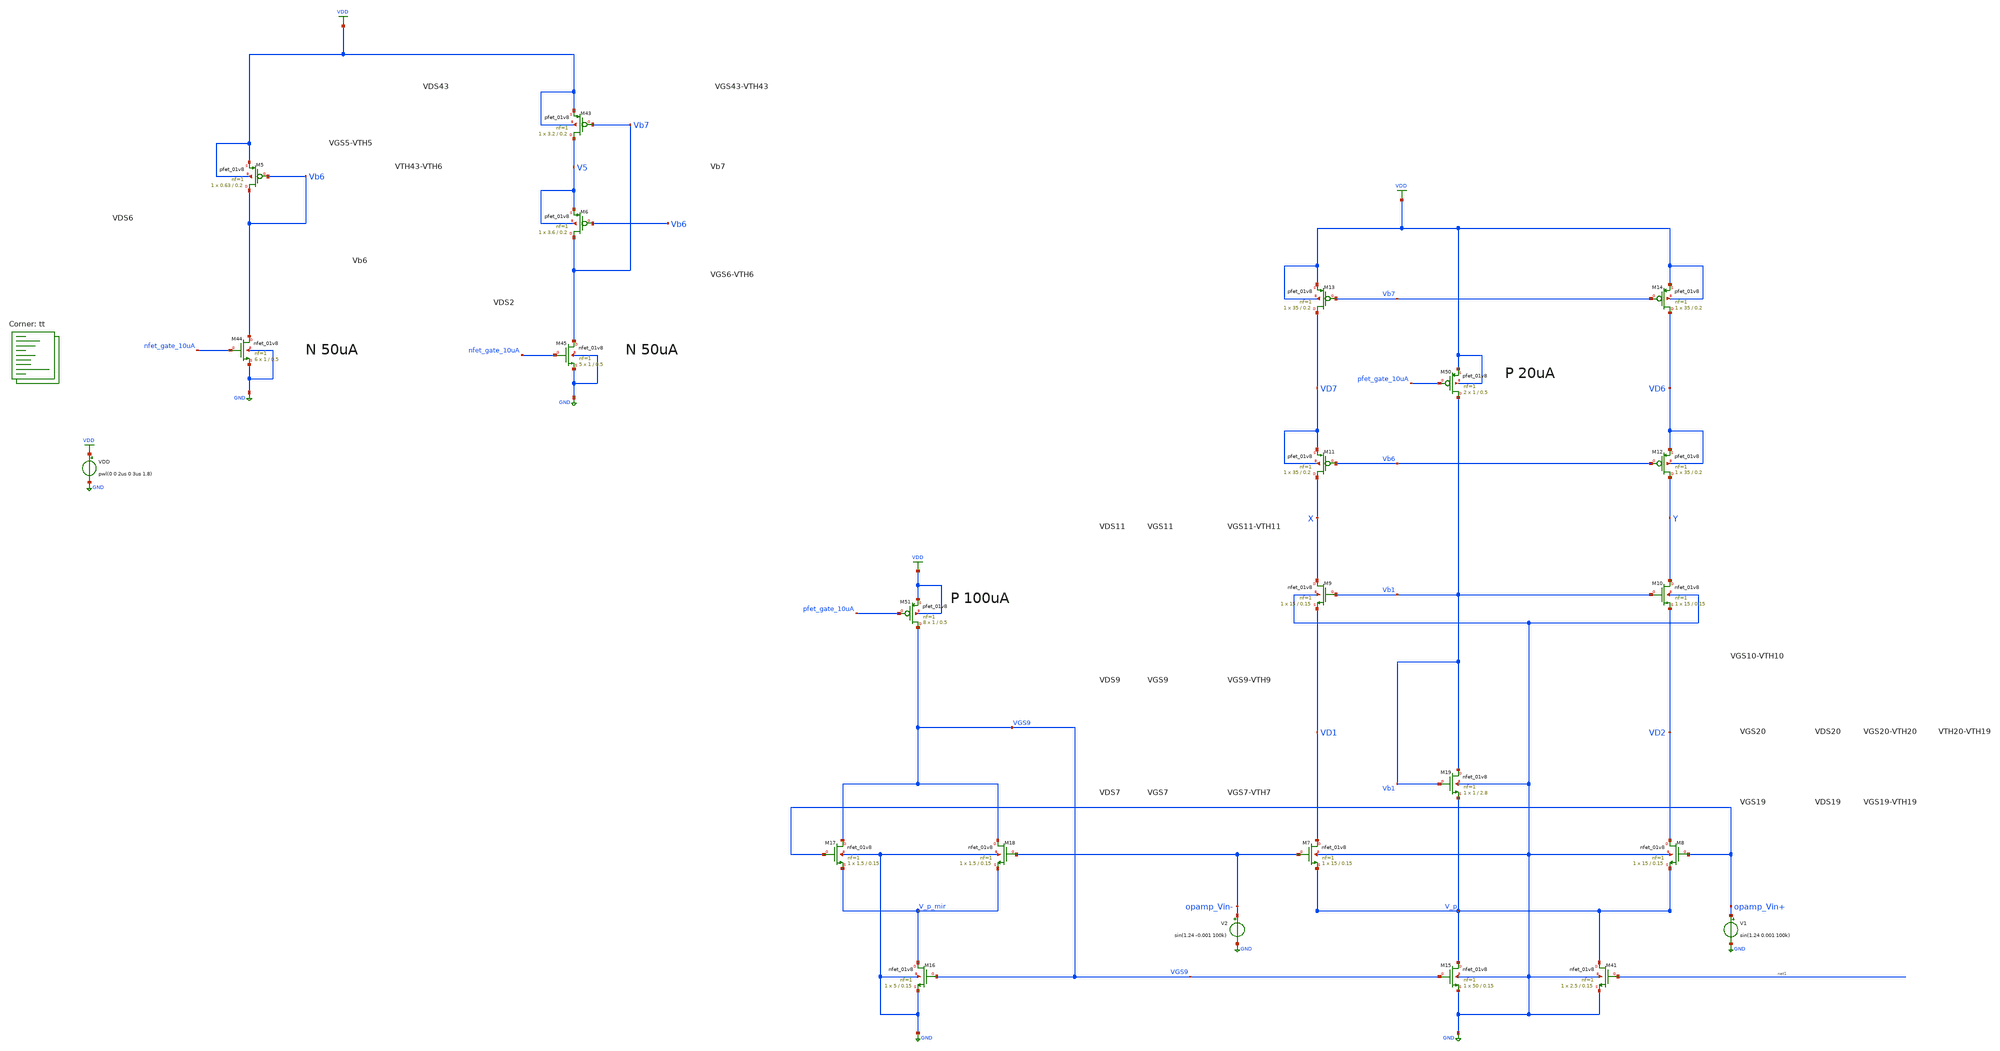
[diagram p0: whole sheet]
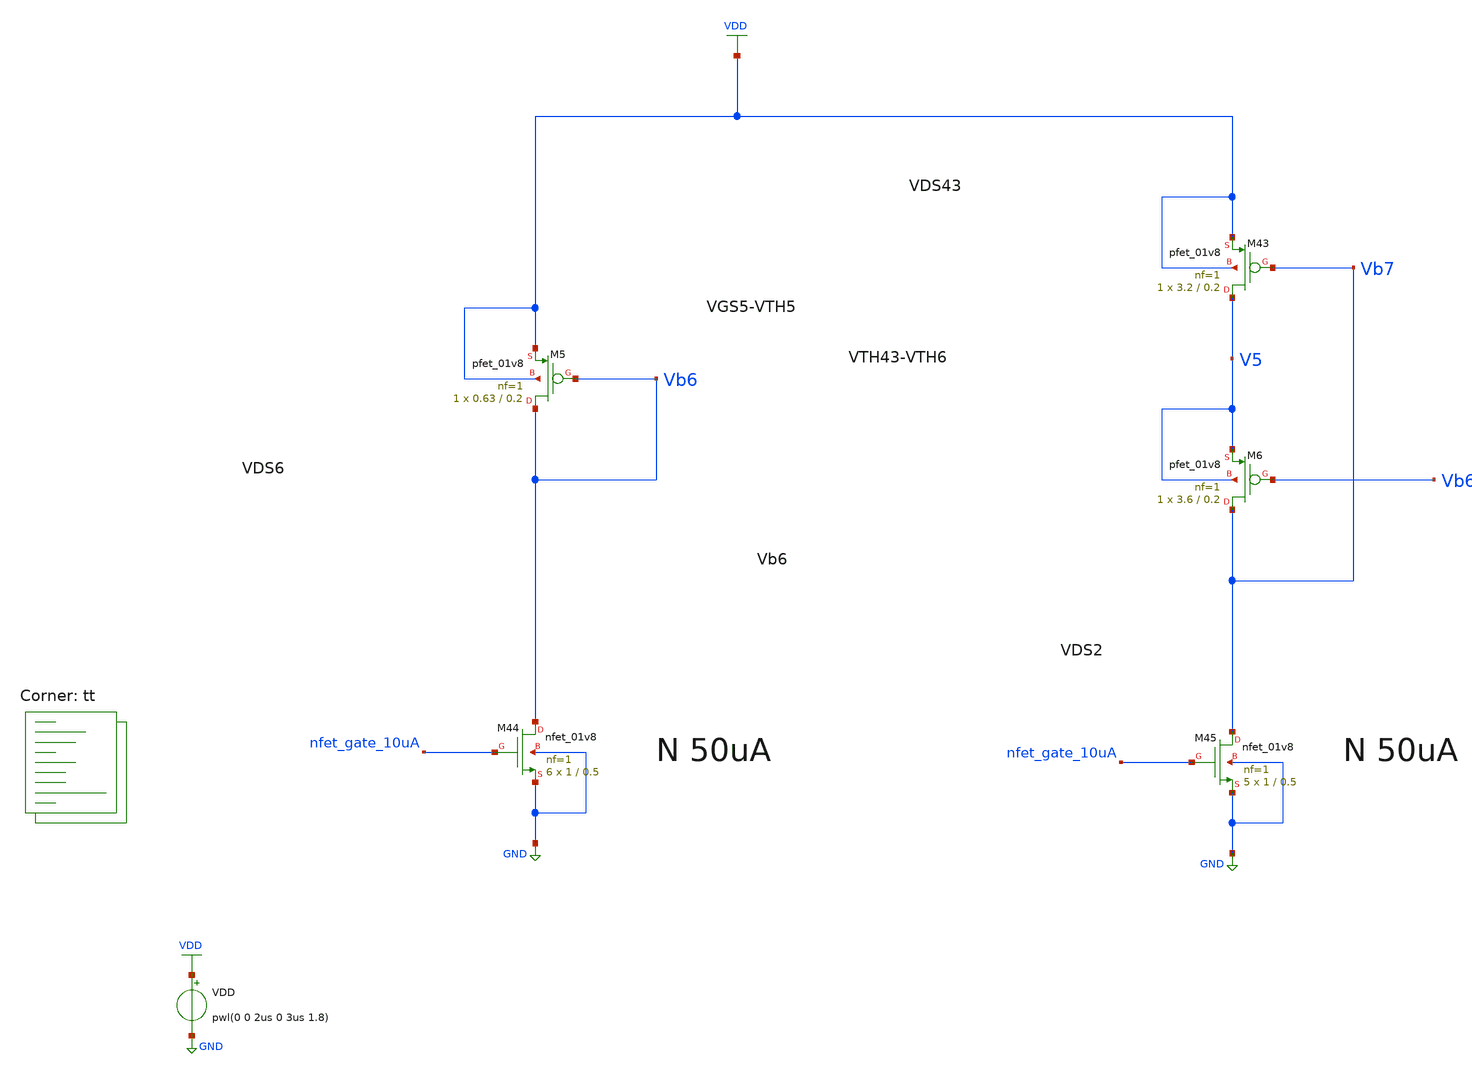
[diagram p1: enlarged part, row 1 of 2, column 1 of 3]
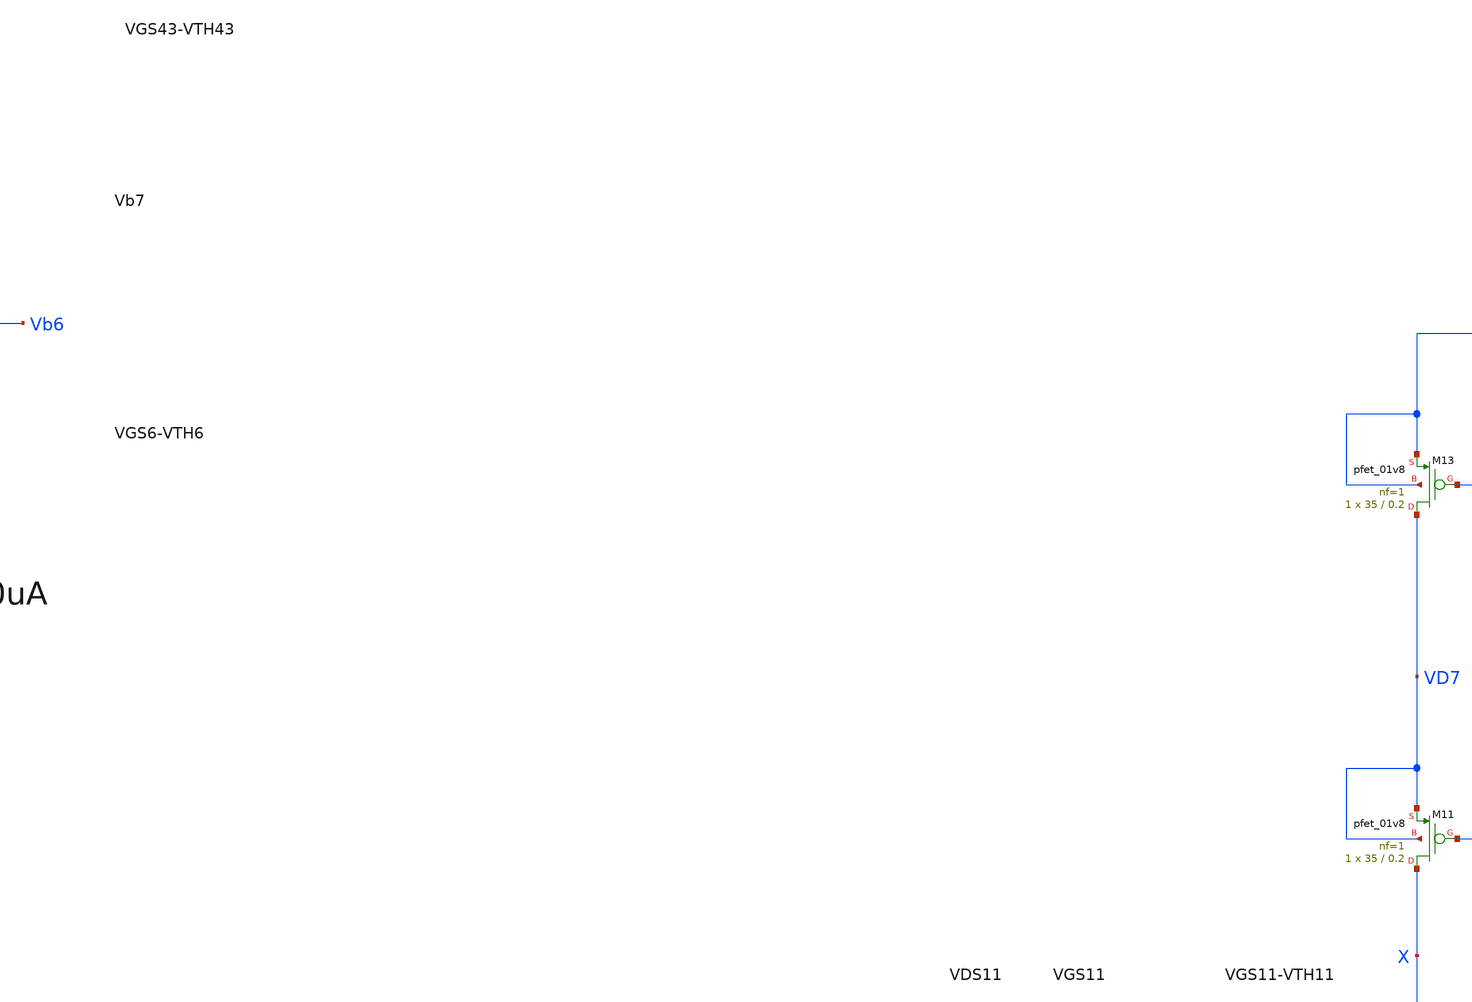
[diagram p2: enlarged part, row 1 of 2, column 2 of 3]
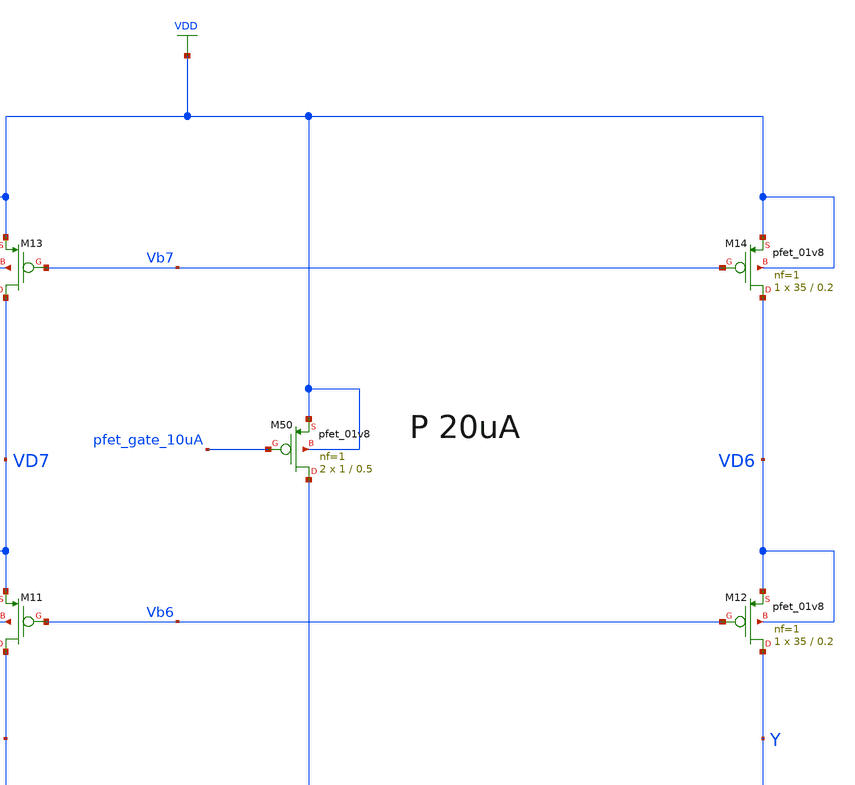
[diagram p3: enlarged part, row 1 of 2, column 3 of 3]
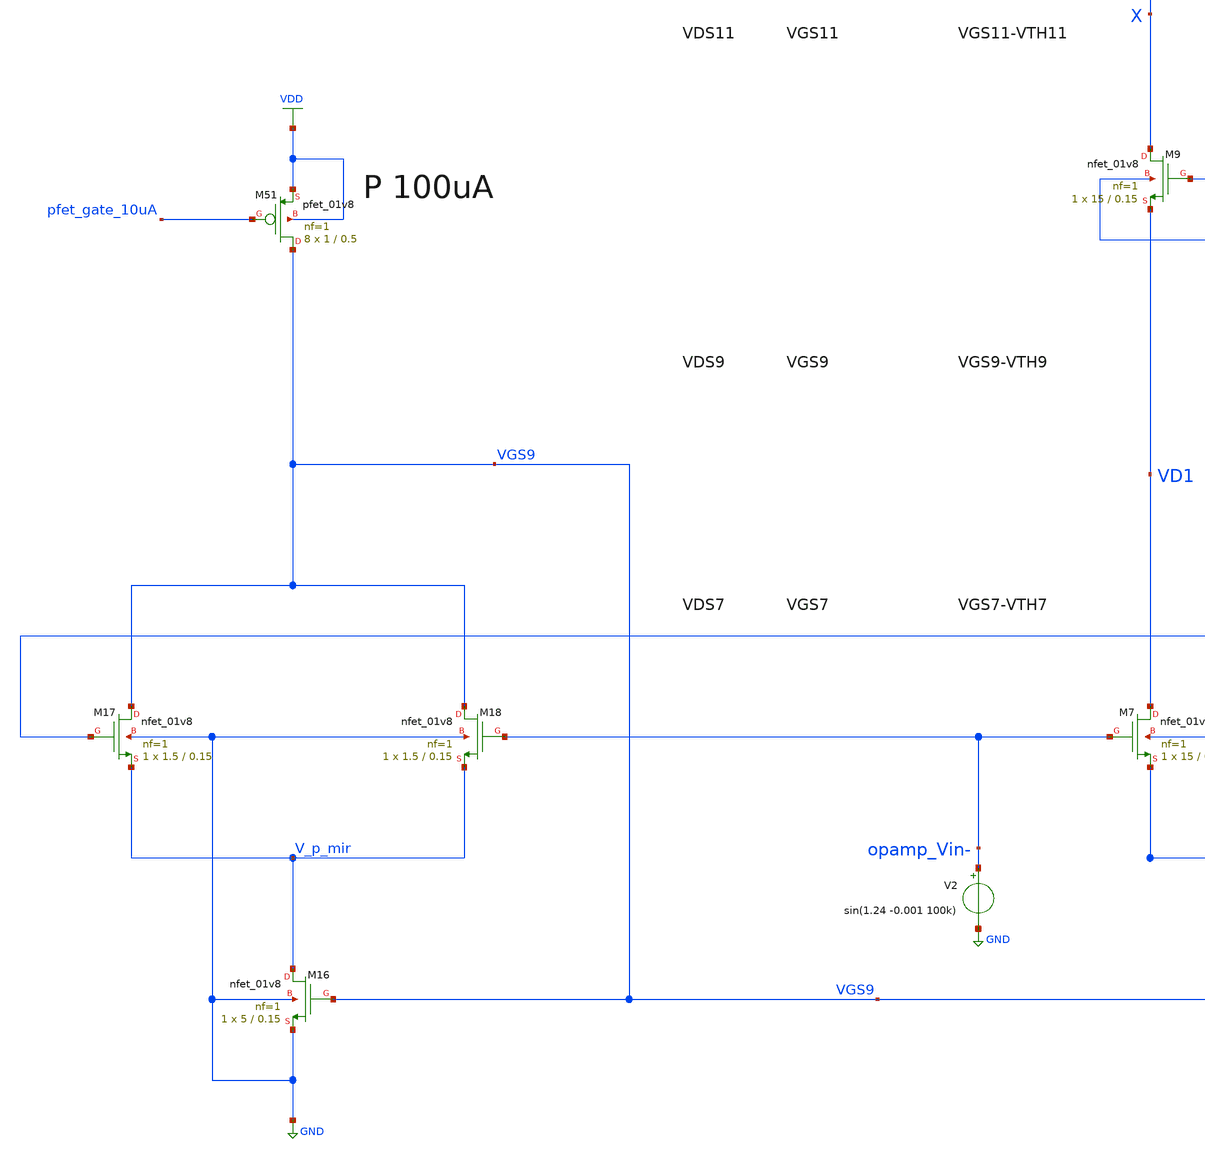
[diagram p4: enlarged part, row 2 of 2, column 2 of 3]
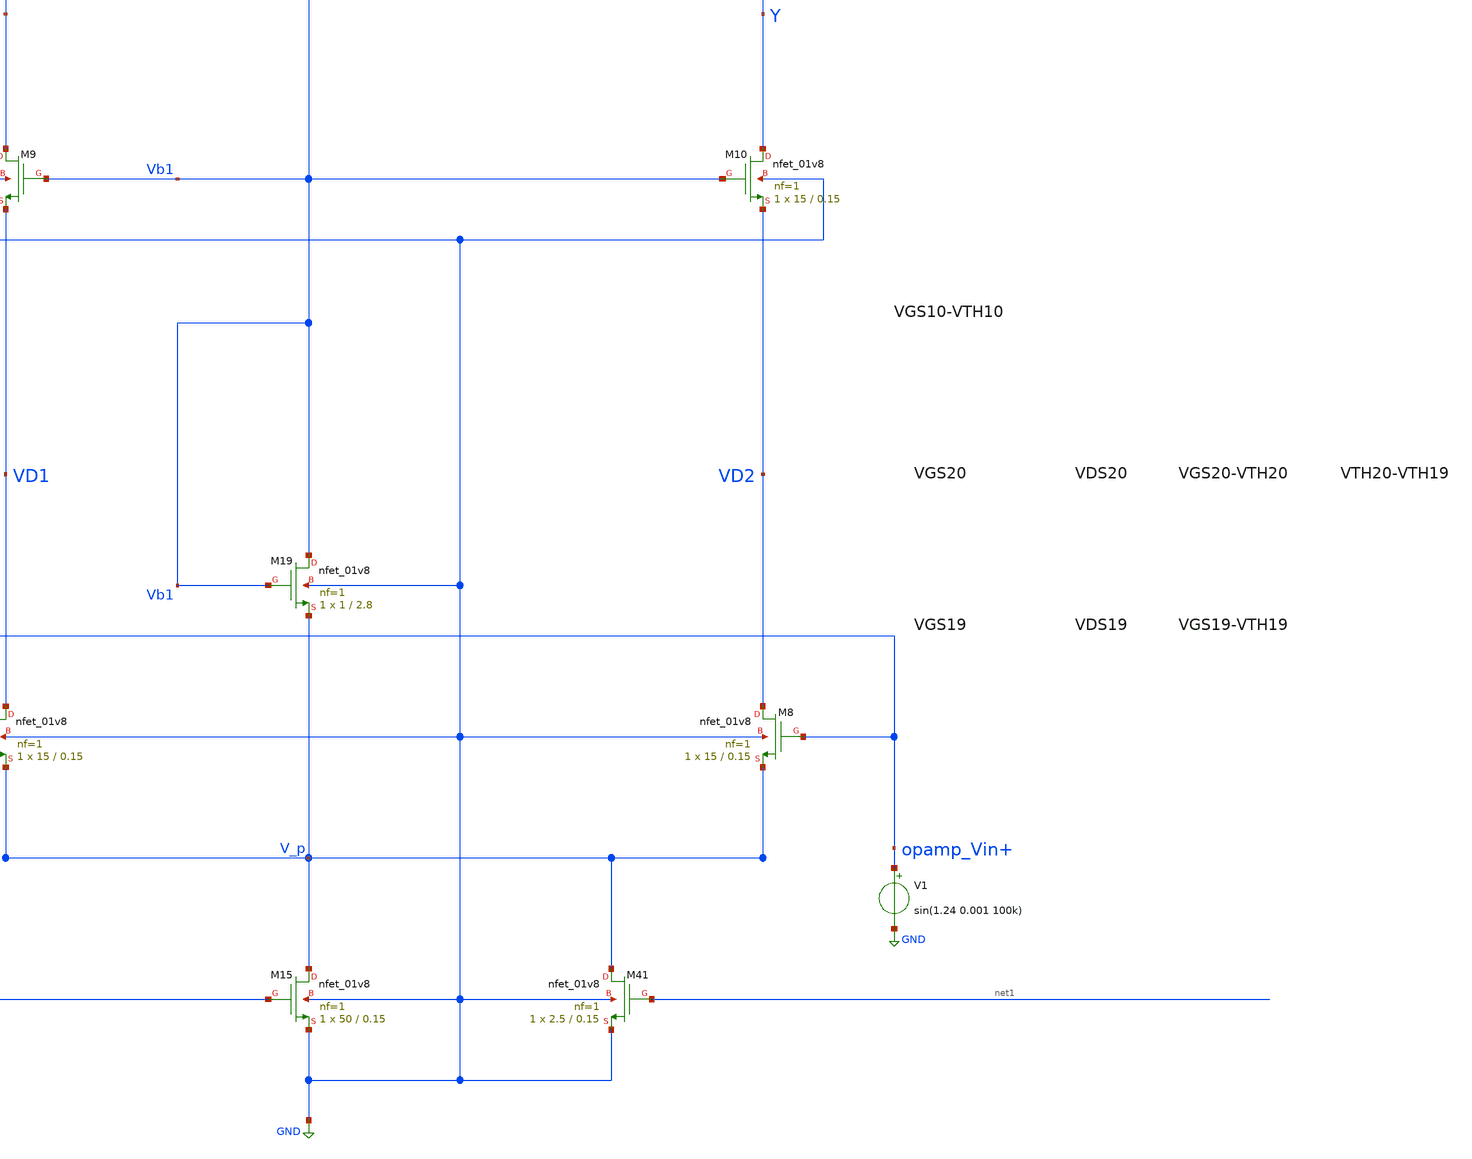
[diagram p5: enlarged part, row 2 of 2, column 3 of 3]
** sch_path: projects/ASU/EEE572/schematic/tb_opamp_full_5_2.sch
**.subckt tb_opamp_full_5_2
VDD VDD GND pwl(0 0 2us 0 3us 1.8)
XM7 VD1 opamp_Vin- V_p GND sky130_fd_pr__nfet_01v8 L=0.15 W=15 nf=1 ad='int((nf+1)/2) * W/nf * 0.29'
+ as='int((nf+2)/2) * W/nf * 0.29' pd='2*int((nf+1)/2) * (W/nf + 0.29)' ps='2*int((nf+2)/2) * (W/nf + 0.29)'
+ nrd='0.29 / W' nrs='0.29 / W' sa=0 sb=0 sd=0 mult=1 m=1
XM8 VD2 opamp_Vin+ V_p GND sky130_fd_pr__nfet_01v8 L=0.15 W=15 nf=1 ad='int((nf+1)/2) * W/nf * 0.29'
+ as='int((nf+2)/2) * W/nf * 0.29' pd='2*int((nf+1)/2) * (W/nf + 0.29)' ps='2*int((nf+2)/2) * (W/nf + 0.29)'
+ nrd='0.29 / W' nrs='0.29 / W' sa=0 sb=0 sd=0 mult=1 m=1
XM9 X Vb1 VD1 GND sky130_fd_pr__nfet_01v8 L=0.15 W=15 nf=1 ad='int((nf+1)/2) * W/nf * 0.29' as='int((nf+2)/2) * W/nf * 0.29'
+ pd='2*int((nf+1)/2) * (W/nf + 0.29)' ps='2*int((nf+2)/2) * (W/nf + 0.29)' nrd='0.29 / W' nrs='0.29 / W'
+ sa=0 sb=0 sd=0 mult=1 m=1
XM10 Y Vb1 VD2 GND sky130_fd_pr__nfet_01v8 L=0.15 W=15 nf=1 ad='int((nf+1)/2) * W/nf * 0.29' as='int((nf+2)/2) * W/nf * 0.29'
+ pd='2*int((nf+1)/2) * (W/nf + 0.29)' ps='2*int((nf+2)/2) * (W/nf + 0.29)' nrd='0.29 / W' nrs='0.29 / W'
+ sa=0 sb=0 sd=0 mult=1 m=1
XM11 X Vb6 VD7 VD7 sky130_fd_pr__pfet_01v8 L=0.2 W=35 nf=1 ad='int((nf+1)/2) * W/nf * 0.29' as='int((nf+2)/2) * W/nf * 0.29'
+ pd='2*int((nf+1)/2) * (W/nf + 0.29)' ps='2*int((nf+2)/2) * (W/nf + 0.29)' nrd='0.29 / W' nrs='0.29 / W'
+ sa=0 sb=0 sd=0 mult=1 m=1
XM12 Y Vb6 VD6 VD6 sky130_fd_pr__pfet_01v8 L=0.2 W=35 nf=1 ad='int((nf+1)/2) * W/nf * 0.29' as='int((nf+2)/2) * W/nf * 0.29'
+ pd='2*int((nf+1)/2) * (W/nf + 0.29)' ps='2*int((nf+2)/2) * (W/nf + 0.29)' nrd='0.29 / W' nrs='0.29 / W'
+ sa=0 sb=0 sd=0 mult=1 m=1
XM13 VD7 Vb7 VDD VDD sky130_fd_pr__pfet_01v8 L=0.2 W=35 nf=1 ad='int((nf+1)/2) * W/nf * 0.29' as='int((nf+2)/2) * W/nf * 0.29'
+ pd='2*int((nf+1)/2) * (W/nf + 0.29)' ps='2*int((nf+2)/2) * (W/nf + 0.29)' nrd='0.29 / W' nrs='0.29 / W'
+ sa=0 sb=0 sd=0 mult=1 m=1
XM14 VD6 Vb7 VDD VDD sky130_fd_pr__pfet_01v8 L=0.2 W=35 nf=1 ad='int((nf+1)/2) * W/nf * 0.29' as='int((nf+2)/2) * W/nf * 0.29'
+ pd='2*int((nf+1)/2) * (W/nf + 0.29)' ps='2*int((nf+2)/2) * (W/nf + 0.29)' nrd='0.29 / W' nrs='0.29 / W'
+ sa=0 sb=0 sd=0 mult=1 m=1
XM15 V_p VGS9 GND GND sky130_fd_pr__nfet_01v8 L=0.15 W=50 nf=1 ad='int((nf+1)/2) * W/nf * 0.29' as='int((nf+2)/2) * W/nf * 0.29'
+ pd='2*int((nf+1)/2) * (W/nf + 0.29)' ps='2*int((nf+2)/2) * (W/nf + 0.29)' nrd='0.29 / W' nrs='0.29 / W'
+ sa=0 sb=0 sd=0 mult=1 m=1
XM16 V_p_mir VGS9 GND GND sky130_fd_pr__nfet_01v8 L=0.15 W=5 nf=1 ad='int((nf+1)/2) * W/nf * 0.29' as='int((nf+2)/2) * W/nf * 0.29'
+ pd='2*int((nf+1)/2) * (W/nf + 0.29)' ps='2*int((nf+2)/2) * (W/nf + 0.29)' nrd='0.29 / W' nrs='0.29 / W'
+ sa=0 sb=0 sd=0 mult=1 m=1
XM17 VGS9 opamp_Vin+ V_p_mir GND sky130_fd_pr__nfet_01v8 L=0.15 W=1.5 nf=1 ad='int((nf+1)/2) * W/nf * 0.29'
+ as='int((nf+2)/2) * W/nf * 0.29' pd='2*int((nf+1)/2) * (W/nf + 0.29)' ps='2*int((nf+2)/2) * (W/nf + 0.29)'
+ nrd='0.29 / W' nrs='0.29 / W' sa=0 sb=0 sd=0 mult=1 m=1
XM18 VGS9 opamp_Vin- V_p_mir GND sky130_fd_pr__nfet_01v8 L=0.15 W=1.5 nf=1 ad='int((nf+1)/2) * W/nf * 0.29'
+ as='int((nf+2)/2) * W/nf * 0.29' pd='2*int((nf+1)/2) * (W/nf + 0.29)' ps='2*int((nf+2)/2) * (W/nf + 0.29)'
+ nrd='0.29 / W' nrs='0.29 / W' sa=0 sb=0 sd=0 mult=1 m=1
XM19 Vb1 Vb1 V_p GND sky130_fd_pr__nfet_01v8 L=2.8 W=1 nf=1 ad='int((nf+1)/2) * W/nf * 0.29' as='int((nf+2)/2) * W/nf * 0.29'
+ pd='2*int((nf+1)/2) * (W/nf + 0.29)' ps='2*int((nf+2)/2) * (W/nf + 0.29)' nrd='0.29 / W' nrs='0.29 / W'
+ sa=0 sb=0 sd=0 mult=1 m=1
V2 opamp_Vin- GND sin(1.24 -0.001 100k)
V1 opamp_Vin+ GND sin(1.24 0.001 100k)
XM41 V_p net1 GND GND sky130_fd_pr__nfet_01v8 L=0.15 W=2.5 nf=1 ad='int((nf+1)/2) * W/nf * 0.29' as='int((nf+2)/2) * W/nf * 0.29'
+ pd='2*int((nf+1)/2) * (W/nf + 0.29)' ps='2*int((nf+2)/2) * (W/nf + 0.29)' nrd='0.29 / W' nrs='0.29 / W'
+ sa=0 sb=0 sd=0 mult=1 m=1
XM5 Vb6 Vb6 VDD VDD sky130_fd_pr__pfet_01v8 L=0.2 W=0.63 nf=1 ad='int((nf+1)/2) * W/nf * 0.29' as='int((nf+2)/2) * W/nf * 0.29'
+ pd='2*int((nf+1)/2) * (W/nf + 0.29)' ps='2*int((nf+2)/2) * (W/nf + 0.29)' nrd='0.29 / W' nrs='0.29 / W'
+ sa=0 sb=0 sd=0 mult=1 m=1
XM6 Vb7 Vb6 V5 V5 sky130_fd_pr__pfet_01v8 L=0.2 W=3.6 nf=1 ad='int((nf+1)/2) * W/nf * 0.29' as='int((nf+2)/2) * W/nf * 0.29'
+ pd='2*int((nf+1)/2) * (W/nf + 0.29)' ps='2*int((nf+2)/2) * (W/nf + 0.29)' nrd='0.29 / W' nrs='0.29 / W'
+ sa=0 sb=0 sd=0 mult=1 m=1
XM43 V5 Vb7 VDD VDD sky130_fd_pr__pfet_01v8 L=0.2 W=3.2 nf=1 ad='int((nf+1)/2) * W/nf * 0.29' as='int((nf+2)/2) * W/nf * 0.29'
+ pd='2*int((nf+1)/2) * (W/nf + 0.29)' ps='2*int((nf+2)/2) * (W/nf + 0.29)' nrd='0.29 / W' nrs='0.29 / W'
+ sa=0 sb=0 sd=0 mult=1 m=1
XM44 Vb6 nfet_gate_10uA GND GND sky130_fd_pr__nfet_01v8 L=0.5 W=1 nf=1 ad='int((nf+1)/2) * W/nf * 0.29'
+ as='int((nf+2)/2) * W/nf * 0.29' pd='2*int((nf+1)/2) * (W/nf + 0.29)' ps='2*int((nf+2)/2) * (W/nf + 0.29)'
+ nrd='0.29 / W' nrs='0.29 / W' sa=0 sb=0 sd=0 mult=6 m=6
XM45 Vb7 nfet_gate_10uA GND GND sky130_fd_pr__nfet_01v8 L=0.5 W=1 nf=1 ad='int((nf+1)/2) * W/nf * 0.29'
+ as='int((nf+2)/2) * W/nf * 0.29' pd='2*int((nf+1)/2) * (W/nf + 0.29)' ps='2*int((nf+2)/2) * (W/nf + 0.29)'
+ nrd='0.29 / W' nrs='0.29 / W' sa=0 sb=0 sd=0 mult=5 m=5
XM50 Vb1 pfet_gate_10uA VDD VDD sky130_fd_pr__pfet_01v8 L=0.5 W=1 nf=1 ad='int((nf+1)/2) * W/nf * 0.29'
+ as='int((nf+2)/2) * W/nf * 0.29' pd='2*int((nf+1)/2) * (W/nf + 0.29)' ps='2*int((nf+2)/2) * (W/nf + 0.29)'
+ nrd='0.29 / W' nrs='0.29 / W' sa=0 sb=0 sd=0 mult=2 m=2
XM51 VGS9 pfet_gate_10uA VDD VDD sky130_fd_pr__pfet_01v8 L=0.5 W=1 nf=1 ad='int((nf+1)/2) * W/nf * 0.29'
+ as='int((nf+2)/2) * W/nf * 0.29' pd='2*int((nf+1)/2) * (W/nf + 0.29)' ps='2*int((nf+2)/2) * (W/nf + 0.29)'
+ nrd='0.29 / W' nrs='0.29 / W' sa=0 sb=0 sd=0 mult=8 m=8
**** begin user architecture code
.lib $::SKYWATER_MODELS/sky130.lib.spice tt



.option method=gear
.option wnflag=1
.option savecurrents

.save @m.x1.xm1.msky130_fd_pr__pfet_01v8[gm] @m.x1.xm1.msky130_fd_pr__pfet_01v8[vth] @m.x1.xm2.msky130_fd_pr__pfet_01v8[gm] @m.x1.xm2.msky130_fd_pr__pfet_01v8[vth] @m.x1.xm3.msky130_fd_pr__pfet_01v8[gm] @m.x1.xm3.msky130_fd_pr__pfet_01v8[vth] @m.x1.xm4.msky130_fd_pr__pfet_01v8[gm] @m.x1.xm4.msky130_fd_pr__pfet_01v8[vth] @m.x1.xm5.msky130_fd_pr__nfet_01v8[gm] @m.x1.xm5.msky130_fd_pr__nfet_01v8[vth] @m.x1.xm6.msky130_fd_pr__pfet_01v8[gm] @m.x1.xm6.msky130_fd_pr__pfet_01v8[vth] @m.x1.xm7.msky130_fd_pr__nfet_01v8[gm] @m.x1.xm7.msky130_fd_pr__nfet_01v8[vth] @m.x1.xm8.msky130_fd_pr__pfet_01v8[gm] @m.x1.xm8.msky130_fd_pr__pfet_01v8[vth] @m.x2.xm2.msky130_fd_pr__nfet_01v8[gm] @m.x2.xm2.msky130_fd_pr__nfet_01v8[vth] @m.x2.xm3.msky130_fd_pr__nfet_01v8[gm] @m.x2.xm3.msky130_fd_pr__nfet_01v8[vth] @m.x2.xm7.msky130_fd_pr__pfet_01v8[gm] @m.x2.xm7.msky130_fd_pr__pfet_01v8[vth] @m.x1.x1.xm1.msky130_fd_pr__nfet_01v8[gm] @m.x1.x1.xm2.msky130_fd_pr__nfet_01v8[gm] @m.x1.x1.xm3.msky130_fd_pr__nfet_01v8[gm] @m.x1.x1.xm4.msky130_fd_pr__nfet_01v8[gm] @m.x1.x1.xm5.msky130_fd_pr__pfet_01v8[gm] @m.x1.x1.xm6.msky130_fd_pr__nfet_01v8[gm] @m.x1.x1.xm7.msky130_fd_pr__pfet_01v8[gm] @m.x1.x2.xm1.msky130_fd_pr__nfet_01v8[gm] @m.x1.x2.xm2.msky130_fd_pr__nfet_01v8[gm] @m.x1.x2.xm3.msky130_fd_pr__nfet_01v8[gm] @m.x1.x2.xm4.msky130_fd_pr__nfet_01v8[gm] @m.x1.x2.xm5.msky130_fd_pr__pfet_01v8[gm] @m.x1.x2.xm6.msky130_fd_pr__nfet_01v8[gm] @m.x1.x2.xm7.msky130_fd_pr__pfet_01v8[gm] @m.xm1.msky130_fd_pr__pfet_01v8[gm] @m.xm1.msky130_fd_pr__pfet_01v8[vth] @m.xm2.msky130_fd_pr__pfet_01v8[gm] @m.xm2.msky130_fd_pr__pfet_01v8[vth] @m.xm3.msky130_fd_pr__pfet_01v8[gm] @m.xm3.msky130_fd_pr__pfet_01v8[vth] @m.xm4.msky130_fd_pr__pfet_01v8[gm] @m.xm4.msky130_fd_pr__pfet_01v8[vth] @m.xm5.msky130_fd_pr__pfet_01v8[gm] @m.xm5.msky130_fd_pr__pfet_01v8[vth] @m.xm6.msky130_fd_pr__pfet_01v8[gm] @m.xm6.msky130_fd_pr__pfet_01v8[vth] @m.xm7.msky130_fd_pr__nfet_01v8[gm] @m.xm7.msky130_fd_pr__nfet_01v8[gds] @m.xm7.msky130_fd_pr__nfet_01v8[vth] @m.xm8.msky130_fd_pr__nfet_01v8[gm] @m.xm8.msky130_fd_pr__nfet_01v8[vth] @m.xm8.msky130_fd_pr__nfet_01v8[gm] @m.xm8.msky130_fd_pr__nfet_01v8[vth] @m.xm9.msky130_fd_pr__nfet_01v8[gm] @m.xm9.msky130_fd_pr__nfet_01v8[gds] @m.xm9.msky130_fd_pr__nfet_01v8[vth] @m.xm10.msky130_fd_pr__nfet_01v8[gm] @m.xm10.msky130_fd_pr__nfet_01v8[vth] @m.xm11.msky130_fd_pr__pfet_01v8[gm] @m.xm11.msky130_fd_pr__pfet_01v8[gds] @m.xm11.msky130_fd_pr__pfet_01v8[vth] @m.xm11.msky130_fd_pr__pfet_01v8[gds] @m.xm12.msky130_fd_pr__pfet_01v8[gm] @m.xm12.msky130_fd_pr__pfet_01v8[vth] @m.xm12.msky130_fd_pr__pfet_01v8[gds] @m.xm13.msky130_fd_pr__pfet_01v8[gm] @m.xm13.msky130_fd_pr__pfet_01v8[gds] @m.xm13.msky130_fd_pr__pfet_01v8[vth] @m.xm13.msky130_fd_pr__pfet_01v8[gds] @m.xm14.msky130_fd_pr__nfet_01v8[gm] @m.xm14.msky130_fd_pr__nfet_01v8[vth] @m.xm14.msky130_fd_pr__pfet_01v8[gds] @m.xm15.msky130_fd_pr__nfet_01v8[gm] @m.xm15.msky130_fd_pr__nfet_01v8[vth] @m.xm16.msky130_fd_pr__nfet_01v8[gm] @m.xm16.msky130_fd_pr__nfet_01v8[vth] @m.xm17.msky130_fd_pr__nfet_01v8[gm] @m.xm17.msky130_fd_pr__nfet_01v8[vth] @m.xm18.msky130_fd_pr__nfet_01v8[gm] @m.xm18.msky130_fd_pr__nfet_01v8[vth] @m.xm19.msky130_fd_pr__nfet_01v8[gm] @m.xm19.msky130_fd_pr__nfet_01v8[vth] @m.xm20.msky130_fd_pr__nfet_01v8[gm] @m.xm20.msky130_fd_pr__nfet_01v8[vth] @m.xm21.msky130_fd_pr__pfet_01v8[gm] @m.xm21.msky130_fd_pr__pfet_01v8[vth] @m.xm22.msky130_fd_pr__pfet_01v8[gm] @m.xm22.msky130_fd_pr__pfet_01v8[vth] @m.xm23.msky130_fd_pr__pfet_01v8[gm] @m.xm23.msky130_fd_pr__pfet_01v8[vth] @m.xm24.msky130_fd_pr__pfet_01v8[gm] @m.xm24.msky130_fd_pr__pfet_01v8[vth] @m.xm25.msky130_fd_pr__nfet_01v8[gm] @m.xm25.msky130_fd_pr__nfet_01v8[vth] @m.xm26.msky130_fd_pr__pfet_01v8[gm] @m.xm26.msky130_fd_pr__pfet_01v8[vth] @m.xm27.msky130_fd_pr__nfet_01v8[gm] @m.xm27.msky130_fd_pr__nfet_01v8[vth] @m.xm28.msky130_fd_pr__pfet_01v8[gm] @m.xm28.msky130_fd_pr__pfet_01v8[vth] @m.xm29.msky130_fd_pr__pfet_01v8[gm] @m.xm29.msky130_fd_pr__pfet_01v8[vth] @m.xm30.msky130_fd_pr__pfet_01v8[gm] @m.xm30.msky130_fd_pr__pfet_01v8[vth] @m.xm31.msky130_fd_pr__nfet_01v8[gm] @m.xm31.msky130_fd_pr__nfet_01v8[vth] @m.xm32.msky130_fd_pr__nfet_01v8[gm] @m.xm32.msky130_fd_pr__nfet_01v8[vth] @m.xm33.msky130_fd_pr__pfet_01v8[gm] @m.xm33.msky130_fd_pr__pfet_01v8[vth] @m.xm34.msky130_fd_pr__pfet_01v8[gm] @m.xm34.msky130_fd_pr__pfet_01v8[vth] @m.xm35.msky130_fd_pr__pfet_01v8[gm] @m.xm35.msky130_fd_pr__pfet_01v8[vth] @m.xm36.msky130_fd_pr__pfet_01v8[gm] @m.xm36.msky130_fd_pr__pfet_01v8[vth] @m.xm37.msky130_fd_pr__nfet_01v8[gm] @m.xm37.msky130_fd_pr__nfet_01v8[vth] @m.xm37.msky130_fd_pr__nfet_01v8[gds] @m.xm38.msky130_fd_pr__nfet_01v8[gm] @m.xm38.msky130_fd_pr__nfet_01v8[vth] @m.xm38.msky130_fd_pr__nfet_01v8[gds] @m.xm39.msky130_fd_pr__pfet_01v8[gm] @m.xm39.msky130_fd_pr__pfet_01v8[vth] @m.xm39.msky130_fd_pr__pfet_01v8[gds] @m.xm40.msky130_fd_pr__pfet_01v8[gm] @m.xm40.msky130_fd_pr__pfet_01v8[vth] @m.xm40.msky130_fd_pr__pfet_01v8[gds] @m.xm41.msky130_fd_pr__nfet_01v8[gm] @m.xm41.msky130_fd_pr__nfet_01v8[vth] @m.xm42.msky130_fd_pr__pfet_01v8[gm] @m.xm42.msky130_fd_pr__pfet_01v8[vth] @m.xm43.msky130_fd_pr__pfet_01v8[gm] @m.xm43.msky130_fd_pr__pfet_01v8[vth] @m.xm44.msky130_fd_pr__nfet_01v8[gm] @m.xm44.msky130_fd_pr__nfet_01v8[vth] @m.xm45.msky130_fd_pr__nfet_01v8[gm] @m.xm45.msky130_fd_pr__nfet_01v8[vth] @m.xm46.msky130_fd_pr__nfet_01v8[gm] @m.xm46.msky130_fd_pr__nfet_01v8[vth] @m.xm47.msky130_fd_pr__nfet_01v8[gm] @m.xm47.msky130_fd_pr__nfet_01v8[vth] @m.xm48.msky130_fd_pr__nfet_01v8[gm] @m.xm48.msky130_fd_pr__nfet_01v8[vth] @m.xm49.msky130_fd_pr__nfet_01v8[gm] @m.xm49.msky130_fd_pr__nfet_01v8[vth] @m.xm52.msky130_fd_pr__pfet_01v8[gm] @m.xm52.msky130_fd_pr__pfet_01v8[vth] @m.xm52.msky130_fd_pr__pfet_01v8[gds] @m.xm63.msky130_fd_pr__pfet_01v8[gm] @m.xm63.msky130_fd_pr__pfet_01v8[vth] @m.xm63.msky130_fd_pr__pfet_01v8[gds]


* .ic v(v_top) = 1.8

.control
  * let runs=3
  * let run=1

  * dowhile run <= runs
    * save v(vout+) v(vout-) v(vin+) v(vin-) v(v_err_amp_ref) v(x2.x) v(x2.y) v(x2.vb1) v(x2.vb2)
+ v(x2.vb3) v(x2.v_tot)
    save all
    remzerovec
    set appendwrite
    * dc temp -40 120 10 VDD 0 4.0 0.2
    * dc VDD 0 2.0 0.02 temp -40 120 40
    * dc V5 0 0.01 0.0001
    tran 2n 30u
    * tran 1p 3n
    * tran 0.1ns 30us
    * ac dec 40 1 10T
    let first_out = x - y
    let second_out = v_out_x - v_out_y
    write tb_opamp_full_5_2.raw
    * reset
    * let run = run + 1
  * end

.endc





**** end user architecture code
**.ends
.GLOBAL GND
.GLOBAL VDD
.end
